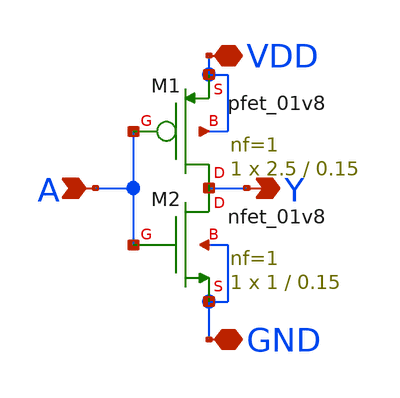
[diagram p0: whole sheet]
** sch_path: inv_test.sch
**.subckt inv_test A Y VDD GND
*.ipin A
*.opin Y
*.iopin VDD
*.iopin GND
XM1 Y A VDD VDD sky130_fd_pr__pfet_01v8 L=0.15 W=2.5 nf=1 ad='int((nf+1)/2) * W/nf * 0.29' as='int((nf+2)/2) * W/nf * 0.29'
+ pd='2*int((nf+1)/2) * (W/nf + 0.29)' ps='2*int((nf+2)/2) * (W/nf + 0.29)' nrd='0.29 / W' nrs='0.29 / W'
+ sa=0 sb=0 sd=0 mult=1 m=1
XM2 Y A GND GND sky130_fd_pr__nfet_01v8 L=0.15 W=1 nf=1 ad='int((nf+1)/2) * W/nf * 0.29' as='int((nf+2)/2) * W/nf * 0.29'
+ pd='2*int((nf+1)/2) * (W/nf + 0.29)' ps='2*int((nf+2)/2) * (W/nf + 0.29)' nrd='0.29 / W' nrs='0.29 / W'
+ sa=0 sb=0 sd=0 mult=1 m=1
**.ends
.end
